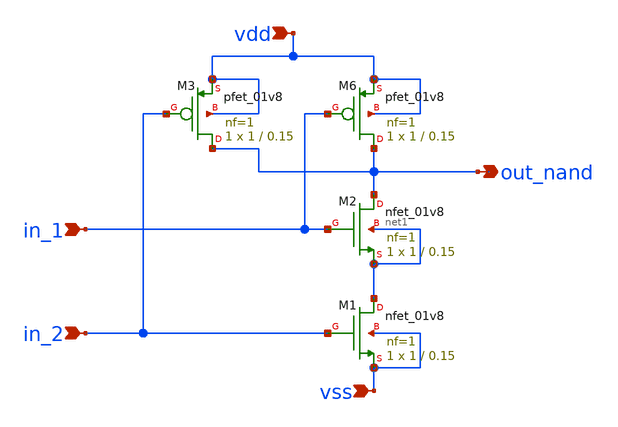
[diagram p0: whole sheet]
** sch_path: projects/custom_lib/nand.sch
**.subckt nand vdd in_1 in_2 vss out_nand
*.ipin vdd
*.ipin in_1
*.ipin in_2
*.ipin vss
*.opin out_nand
XM1 net1 in_2 vss vss sky130_fd_pr__nfet_01v8 L=0.15 W=1 nf=1 ad='int((nf+1)/2) * W/nf * 0.29' as='int((nf+2)/2) * W/nf * 0.29'
+ pd='2*int((nf+1)/2) * (W/nf + 0.29)' ps='2*int((nf+2)/2) * (W/nf + 0.29)' nrd='0.29 / W' nrs='0.29 / W'
+ sa=0 sb=0 sd=0 mult=1 m=1
XM2 out_nand in_1 net1 net1 sky130_fd_pr__nfet_01v8 L=0.15 W=1 nf=1 ad='int((nf+1)/2) * W/nf * 0.29'
+ as='int((nf+2)/2) * W/nf * 0.29' pd='2*int((nf+1)/2) * (W/nf + 0.29)' ps='2*int((nf+2)/2) * (W/nf + 0.29)'
+ nrd='0.29 / W' nrs='0.29 / W' sa=0 sb=0 sd=0 mult=1 m=1
XM6 out_nand in_1 vdd vdd sky130_fd_pr__pfet_01v8 L=0.15 W=1 nf=1 ad='int((nf+1)/2) * W/nf * 0.29' as='int((nf+2)/2) * W/nf * 0.29'
+ pd='2*int((nf+1)/2) * (W/nf + 0.29)' ps='2*int((nf+2)/2) * (W/nf + 0.29)' nrd='0.29 / W' nrs='0.29 / W'
+ sa=0 sb=0 sd=0 mult=1 m=1
XM3 out_nand in_2 vdd vdd sky130_fd_pr__pfet_01v8 L=0.15 W=1 nf=1 ad='int((nf+1)/2) * W/nf * 0.29' as='int((nf+2)/2) * W/nf * 0.29'
+ pd='2*int((nf+1)/2) * (W/nf + 0.29)' ps='2*int((nf+2)/2) * (W/nf + 0.29)' nrd='0.29 / W' nrs='0.29 / W'
+ sa=0 sb=0 sd=0 mult=1 m=1
**.ends
.end
